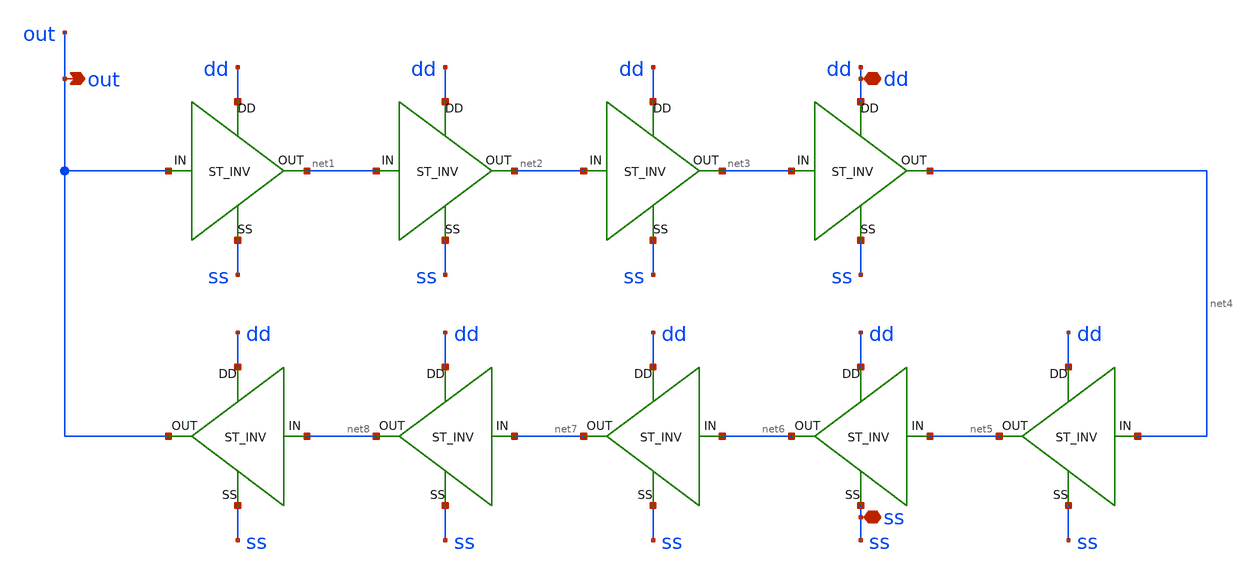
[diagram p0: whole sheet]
** sch_path: xschem/ring_100mV_st.sch
**.subckt ring_100mV_st dd ss out
*.iopin dd
*.iopin ss
*.opin out
X2 out net1 dd ss st_inv
X1 net1 net2 dd ss st_inv
X3 net2 net3 dd ss st_inv
X4 net3 net4 dd ss st_inv
X10 net4 net5 dd ss st_inv
X11 net5 net6 dd ss st_inv
X12 net6 net7 dd ss st_inv
X13 net7 net8 dd ss st_inv
X14 net8 out dd ss st_inv
**.ends

* expanding   symbol:  st_inv.sym # of pins=4
** sym_path: xschem/st_inv.sym
** sch_path: xschem/st_inv.sch
.subckt st_inv IN OUT DD SS
*.ipin IN
*.iopin DD
*.iopin SS
*.opin OUT
XM5 OUT IN net1 SS sky130_fd_pr__nfet_01v8_lvt L=0.8 W=5.5 nf=1 ad='int((nf+1)/2) * W/nf * 0.29' as='int((nf+2)/2) * W/nf * 0.29'
+ pd='2*int((nf+1)/2) * (W/nf + 0.29)' ps='2*int((nf+2)/2) * (W/nf + 0.29)' nrd='0.29 / W' nrs='0.29 / W'
+ sa=0 sb=0 sd=0 mult=4 m=4
XM10 OUT IN net2 DD sky130_fd_pr__pfet_01v8_lvt L=0.8 W=1 nf=1 ad='int((nf+1)/2) * W/nf * 0.29' as='int((nf+2)/2) * W/nf * 0.29'
+ pd='2*int((nf+1)/2) * (W/nf + 0.29)' ps='2*int((nf+2)/2) * (W/nf + 0.29)' nrd='0.29 / W' nrs='0.29 / W'
+ sa=0 sb=0 sd=0 mult=1 m=1
XM11 net1 IN SS SS sky130_fd_pr__nfet_01v8_lvt L=0.8 W=5.5 nf=1 ad='int((nf+1)/2) * W/nf * 0.29' as='int((nf+2)/2) * W/nf * 0.29'
+ pd='2*int((nf+1)/2) * (W/nf + 0.29)' ps='2*int((nf+2)/2) * (W/nf + 0.29)' nrd='0.29 / W' nrs='0.29 / W'
+ sa=0 sb=0 sd=0 mult=8 m=8
XM12 DD OUT net1 SS sky130_fd_pr__nfet_01v8_lvt L=0.8 W=5.5 nf=1 ad='int((nf+1)/2) * W/nf * 0.29' as='int((nf+2)/2) * W/nf * 0.29'
+ pd='2*int((nf+1)/2) * (W/nf + 0.29)' ps='2*int((nf+2)/2) * (W/nf + 0.29)' nrd='0.29 / W' nrs='0.29 / W'
+ sa=0 sb=0 sd=0 mult=4 m=4
XM13 net2 IN DD DD sky130_fd_pr__pfet_01v8_lvt L=0.8 W=1 nf=1 ad='int((nf+1)/2) * W/nf * 0.29' as='int((nf+2)/2) * W/nf * 0.29'
+ pd='2*int((nf+1)/2) * (W/nf + 0.29)' ps='2*int((nf+2)/2) * (W/nf + 0.29)' nrd='0.29 / W' nrs='0.29 / W'
+ sa=0 sb=0 sd=0 mult=2 m=2
XM14 SS OUT net2 DD sky130_fd_pr__pfet_01v8_lvt L=0.8 W=1 nf=1 ad='int((nf+1)/2) * W/nf * 0.29' as='int((nf+2)/2) * W/nf * 0.29'
+ pd='2*int((nf+1)/2) * (W/nf + 0.29)' ps='2*int((nf+2)/2) * (W/nf + 0.29)' nrd='0.29 / W' nrs='0.29 / W'
+ sa=0 sb=0 sd=0 mult=1 m=1
.ends

.end
